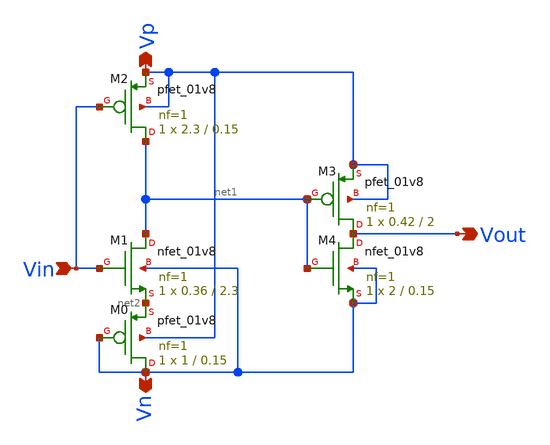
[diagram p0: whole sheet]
** sch_path: xschem/Vth_sch/Symbol/th13_backup.sch
**.subckt th13_backup Vn Vp Vin Vout
*.opin Vn
*.opin Vp
*.ipin Vin
*.opin Vout
XM3 Vout net1 Vp Vp sky130_fd_pr__pfet_01v8 L=2 W=0.42 nf=1 ad='int((nf+1)/2) * W/nf * 0.29' as='int((nf+2)/2) * W/nf * 0.29'
+ pd='2*int((nf+1)/2) * (W/nf + 0.29)' ps='2*int((nf+2)/2) * (W/nf + 0.29)' nrd='0.29 / W' nrs='0.29 / W'
+ sa=0 sb=0 sd=0 mult=1 m=1
XM4 Vout net1 Vn Vn sky130_fd_pr__nfet_01v8 L=0.15 W=2 nf=1 ad='int((nf+1)/2) * W/nf * 0.29' as='int((nf+2)/2) * W/nf * 0.29'
+ pd='2*int((nf+1)/2) * (W/nf + 0.29)' ps='2*int((nf+2)/2) * (W/nf + 0.29)' nrd='0.29 / W' nrs='0.29 / W'
+ sa=0 sb=0 sd=0 mult=1 m=1
XM2 net1 Vin Vp Vp sky130_fd_pr__pfet_01v8 L=0.15 W=2.3 nf=1 ad='int((nf+1)/2) * W/nf * 0.29' as='int((nf+2)/2) * W/nf * 0.29'
+ pd='2*int((nf+1)/2) * (W/nf + 0.29)' ps='2*int((nf+2)/2) * (W/nf + 0.29)' nrd='0.29 / W' nrs='0.29 / W'
+ sa=0 sb=0 sd=0 mult=1 m=1
XM1 net1 Vin net2 Vn sky130_fd_pr__nfet_01v8 L=2.3 W=0.36 nf=1 ad='int((nf+1)/2) * W/nf * 0.29' as='int((nf+2)/2) * W/nf * 0.29'
+ pd='2*int((nf+1)/2) * (W/nf + 0.29)' ps='2*int((nf+2)/2) * (W/nf + 0.29)' nrd='0.29 / W' nrs='0.29 / W'
+ sa=0 sb=0 sd=0 mult=1 m=1
XM0 Vn Vn net2 Vp sky130_fd_pr__pfet_01v8 L=0.15 W=1 nf=1 ad='int((nf+1)/2) * W/nf * 0.29' as='int((nf+2)/2) * W/nf * 0.29'
+ pd='2*int((nf+1)/2) * (W/nf + 0.29)' ps='2*int((nf+2)/2) * (W/nf + 0.29)' nrd='0.29 / W' nrs='0.29 / W'
+ sa=0 sb=0 sd=0 mult=1 m=1
**.ends
.end
